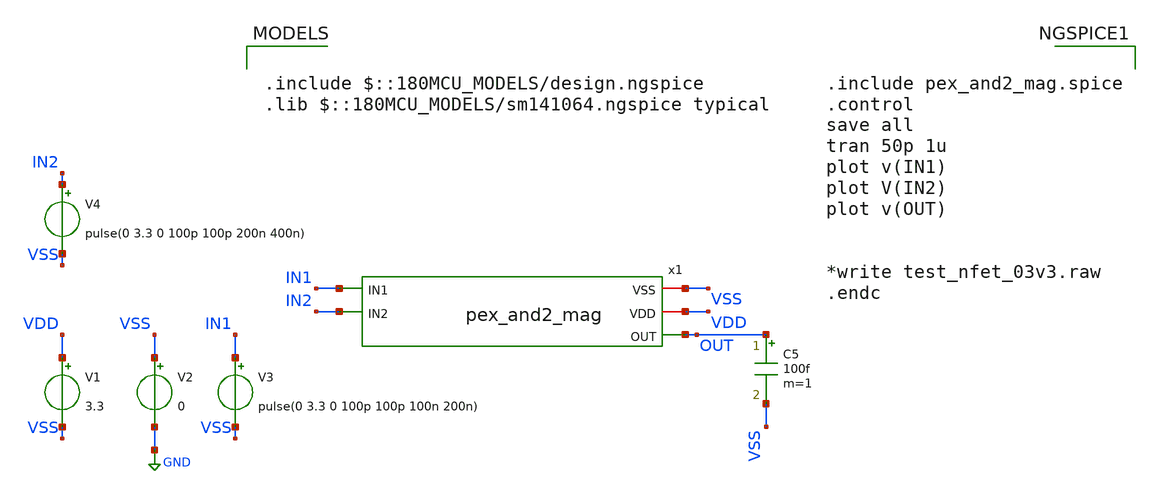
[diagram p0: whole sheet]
** sch_path: Clock_Generator_PAKISTAN_02/xschem/and_test_pex.sch
**.subckt and_test_pex
V1 VDD VSS 3.3
V2 VSS GND 0
V3 IN1 VSS pulse(0 3.3 0 100p 100p 100n 200n)
V4 IN2 VSS pulse(0 3.3 0 100p 100p 200n 400n)
C5 OUT VSS 100f m=1
x1 IN1 VSS VDD OUT IN2 pex_and2_mag
**** begin user architecture code

.include $::180MCU_MODELS/design.ngspice
.lib $::180MCU_MODELS/sm141064.ngspice typical



.include pex_and2_mag.spice
.control
save all
tran 50p 1u
plot v(IN1)
plot V(IN2)
plot v(OUT)


*write test_nfet_03v3.raw
.endc


**** end user architecture code
**.ends
.GLOBAL GND
.end
